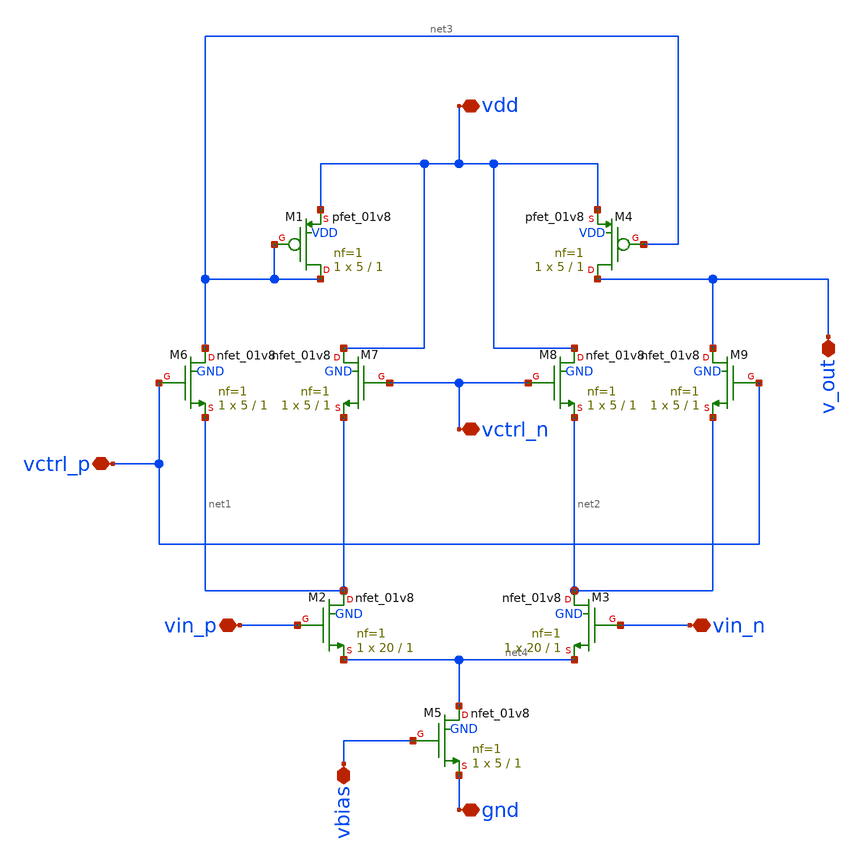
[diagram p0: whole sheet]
** sch_path: ISSCC27/submitted_notebooks/subthreshold_vga_gmid/schematic/vga_core_9t.sch
**.subckt vga_core_9t vdd vin_n vbias vctrl_n gnd vctrl_p vin_p v_out
*.iopin vdd
*.iopin vin_n
*.iopin vbias
*.iopin vctrl_n
*.iopin gnd
*.iopin vctrl_p
*.iopin vin_p
*.iopin v_out
XM1 net3 net3 vdd VDD sky130_fd_pr__pfet_01v8 L=1 W=5 nf=1 ad='int((1 + 1)/2) * 5 / 1 * 0.29' as='int((1 + 2)/2) * 5 / 1 * 0.29'
+ pd='2*int((1 + 1)/2) * (5 / 1 + 0.29)' ps='2*int((1 + 2)/2) * (5 / 1 + 0.29)' nrd='0.29 / 5 ' nrs='0.29 / 5 '
+ sa=0 sb=0 sd=0 mult=1 m=1
XM2 net1 vin_p net4 GND sky130_fd_pr__nfet_01v8 L=1 W=20 nf=1 ad='int((1 + 1)/2) * 20 / 1 * 0.29' as='int((1 + 2)/2) * 20 / 1 * 0.29'
+ pd='2*int((1 + 1)/2) * (20 / 1 + 0.29)' ps='2*int((1 + 2)/2) * (20 / 1 + 0.29)' nrd='0.29 / 20 ' nrs='0.29 / 20 '
+ sa=0 sb=0 sd=0 mult=1 m=1
XM3 net2 vin_n net4 GND sky130_fd_pr__nfet_01v8 L=1 W=20 nf=1 ad='int((1 + 1)/2) * 20 / 1 * 0.29' as='int((1 + 2)/2) * 20 / 1 * 0.29'
+ pd='2*int((1 + 1)/2) * (20 / 1 + 0.29)' ps='2*int((1 + 2)/2) * (20 / 1 + 0.29)' nrd='0.29 / 20 ' nrs='0.29 / 20 '
+ sa=0 sb=0 sd=0 mult=1 m=1
XM4 v_out net3 vdd VDD sky130_fd_pr__pfet_01v8 L=1 W=5 nf=1 ad='int((1 + 1)/2) * 5 / 1 * 0.29' as='int((1 + 2)/2) * 5 / 1 * 0.29'
+ pd='2*int((1 + 1)/2) * (5 / 1 + 0.29)' ps='2*int((1 + 2)/2) * (5 / 1 + 0.29)' nrd='0.29 / 5 ' nrs='0.29 / 5 '
+ sa=0 sb=0 sd=0 mult=1 m=1
XM5 net4 vbias gnd GND sky130_fd_pr__nfet_01v8 L=1 W=5 nf=1 ad='int((1 + 1)/2) * 5 / 1 * 0.29' as='int((1 + 2)/2) * 5 / 1 * 0.29'
+ pd='2*int((1 + 1)/2) * (5 / 1 + 0.29)' ps='2*int((1 + 2)/2) * (5 / 1 + 0.29)' nrd='0.29 / 5 ' nrs='0.29 / 5 '
+ sa=0 sb=0 sd=0 mult=1 m=1
XM6 net3 vctrl_p net1 GND sky130_fd_pr__nfet_01v8 L=1 W=5 nf=1 ad='int((1 + 1)/2) * 5 / 1 * 0.29' as='int((1 + 2)/2) * 5 / 1 * 0.29'
+ pd='2*int((1 + 1)/2) * (5 / 1 + 0.29)' ps='2*int((1 + 2)/2) * (5 / 1 + 0.29)' nrd='0.29 / 5 ' nrs='0.29 / 5 '
+ sa=0 sb=0 sd=0 mult=1 m=1
XM7 vdd vctrl_n net1 GND sky130_fd_pr__nfet_01v8 L=1 W=5 nf=1 ad='int((1 + 1)/2) * 5 / 1 * 0.29' as='int((1 + 2)/2) * 5 / 1 * 0.29'
+ pd='2*int((1 + 1)/2) * (5 / 1 + 0.29)' ps='2*int((1 + 2)/2) * (5 / 1 + 0.29)' nrd='0.29 / 5 ' nrs='0.29 / 5 '
+ sa=0 sb=0 sd=0 mult=1 m=1
XM8 vdd vctrl_n net2 GND sky130_fd_pr__nfet_01v8 L=1 W=5 nf=1 ad='int((1 + 1)/2) * 5 / 1 * 0.29' as='int((1 + 2)/2) * 5 / 1 * 0.29'
+ pd='2*int((1 + 1)/2) * (5 / 1 + 0.29)' ps='2*int((1 + 2)/2) * (5 / 1 + 0.29)' nrd='0.29 / 5 ' nrs='0.29 / 5 '
+ sa=0 sb=0 sd=0 mult=1 m=1
XM9 v_out vctrl_p net2 GND sky130_fd_pr__nfet_01v8 L=1 W=5 nf=1 ad='int((1 + 1)/2) * 5 / 1 * 0.29' as='int((1 + 2)/2) * 5 / 1 * 0.29'
+ pd='2*int((1 + 1)/2) * (5 / 1 + 0.29)' ps='2*int((1 + 2)/2) * (5 / 1 + 0.29)' nrd='0.29 / 5 ' nrs='0.29 / 5 '
+ sa=0 sb=0 sd=0 mult=1 m=1
**.ends
.end
